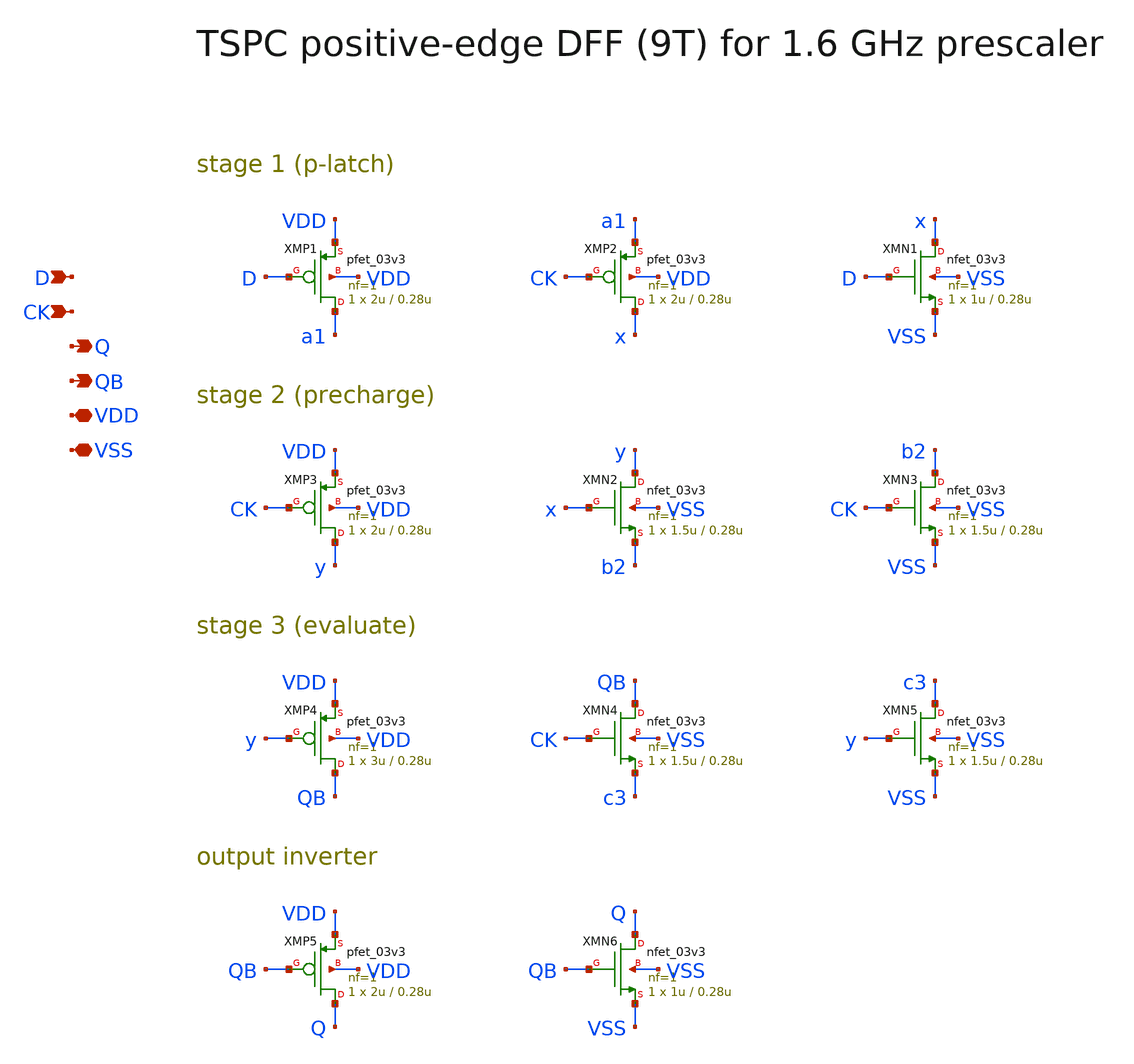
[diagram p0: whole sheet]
** sch_path: v1_claude/xschem/tspc_dff.sch
**.subckt tspc_dff D CK Q QB VDD VSS
*.ipin D
*.ipin CK
*.opin Q
*.opin QB
*.iopin VDD
*.iopin VSS
XMP1 a1 D VDD VDD pfet_03v3 L=0.28u W=2u nf=1 ad='int((nf+1)/2) * W/nf * 0.18u' as='int((nf+2)/2) * W/nf * 0.18u'
+ pd='2*int((nf+1)/2) * (W/nf + 0.18u)' ps='2*int((nf+2)/2) * (W/nf + 0.18u)' nrd='0.18u / W' nrs='0.18u / W'
+ sa=0 sb=0 sd=0 m=1
XMP2 x CK a1 VDD pfet_03v3 L=0.28u W=2u nf=1 ad='int((nf+1)/2) * W/nf * 0.18u' as='int((nf+2)/2) * W/nf * 0.18u'
+ pd='2*int((nf+1)/2) * (W/nf + 0.18u)' ps='2*int((nf+2)/2) * (W/nf + 0.18u)' nrd='0.18u / W' nrs='0.18u / W'
+ sa=0 sb=0 sd=0 m=1
XMN1 x D VSS VSS nfet_03v3 L=0.28u W=1u nf=1 ad='int((nf+1)/2) * W/nf * 0.18u' as='int((nf+2)/2) * W/nf * 0.18u'
+ pd='2*int((nf+1)/2) * (W/nf + 0.18u)' ps='2*int((nf+2)/2) * (W/nf + 0.18u)' nrd='0.18u / W' nrs='0.18u / W'
+ sa=0 sb=0 sd=0 m=1
XMP3 y CK VDD VDD pfet_03v3 L=0.28u W=2u nf=1 ad='int((nf+1)/2) * W/nf * 0.18u' as='int((nf+2)/2) * W/nf * 0.18u'
+ pd='2*int((nf+1)/2) * (W/nf + 0.18u)' ps='2*int((nf+2)/2) * (W/nf + 0.18u)' nrd='0.18u / W' nrs='0.18u / W'
+ sa=0 sb=0 sd=0 m=1
XMN2 y x b2 VSS nfet_03v3 L=0.28u W=1.5u nf=1 ad='int((nf+1)/2) * W/nf * 0.18u' as='int((nf+2)/2) * W/nf * 0.18u'
+ pd='2*int((nf+1)/2) * (W/nf + 0.18u)' ps='2*int((nf+2)/2) * (W/nf + 0.18u)' nrd='0.18u / W' nrs='0.18u / W'
+ sa=0 sb=0 sd=0 m=1
XMN3 b2 CK VSS VSS nfet_03v3 L=0.28u W=1.5u nf=1 ad='int((nf+1)/2) * W/nf * 0.18u' as='int((nf+2)/2) * W/nf * 0.18u'
+ pd='2*int((nf+1)/2) * (W/nf + 0.18u)' ps='2*int((nf+2)/2) * (W/nf + 0.18u)' nrd='0.18u / W' nrs='0.18u / W'
+ sa=0 sb=0 sd=0 m=1
XMP4 QB y VDD VDD pfet_03v3 L=0.28u W=3u nf=1 ad='int((nf+1)/2) * W/nf * 0.18u' as='int((nf+2)/2) * W/nf * 0.18u'
+ pd='2*int((nf+1)/2) * (W/nf + 0.18u)' ps='2*int((nf+2)/2) * (W/nf + 0.18u)' nrd='0.18u / W' nrs='0.18u / W'
+ sa=0 sb=0 sd=0 m=1
XMN4 QB CK c3 VSS nfet_03v3 L=0.28u W=1.5u nf=1 ad='int((nf+1)/2) * W/nf * 0.18u' as='int((nf+2)/2) * W/nf * 0.18u'
+ pd='2*int((nf+1)/2) * (W/nf + 0.18u)' ps='2*int((nf+2)/2) * (W/nf + 0.18u)' nrd='0.18u / W' nrs='0.18u / W'
+ sa=0 sb=0 sd=0 m=1
XMN5 c3 y VSS VSS nfet_03v3 L=0.28u W=1.5u nf=1 ad='int((nf+1)/2) * W/nf * 0.18u' as='int((nf+2)/2) * W/nf * 0.18u'
+ pd='2*int((nf+1)/2) * (W/nf + 0.18u)' ps='2*int((nf+2)/2) * (W/nf + 0.18u)' nrd='0.18u / W' nrs='0.18u / W'
+ sa=0 sb=0 sd=0 m=1
XMP5 Q QB VDD VDD pfet_03v3 L=0.28u W=2u nf=1 ad='int((nf+1)/2) * W/nf * 0.18u' as='int((nf+2)/2) * W/nf * 0.18u'
+ pd='2*int((nf+1)/2) * (W/nf + 0.18u)' ps='2*int((nf+2)/2) * (W/nf + 0.18u)' nrd='0.18u / W' nrs='0.18u / W'
+ sa=0 sb=0 sd=0 m=1
XMN6 Q QB VSS VSS nfet_03v3 L=0.28u W=1u nf=1 ad='int((nf+1)/2) * W/nf * 0.18u' as='int((nf+2)/2) * W/nf * 0.18u'
+ pd='2*int((nf+1)/2) * (W/nf + 0.18u)' ps='2*int((nf+2)/2) * (W/nf + 0.18u)' nrd='0.18u / W' nrs='0.18u / W'
+ sa=0 sb=0 sd=0 m=1
**.ends
.end
